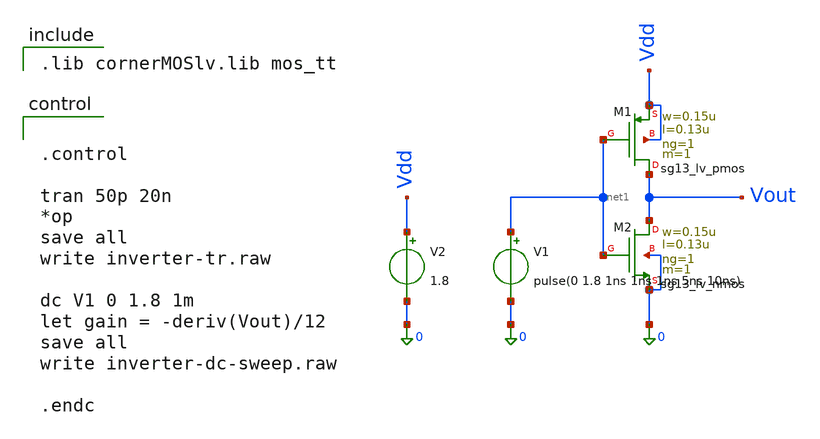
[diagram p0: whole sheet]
** sch_path: designs/inverter/inverter.sch
**.subckt inverter
XM1 Vout net1 Vdd Vdd sg13_lv_pmos w=0.15u l=0.13u ng=1 m=1 mm_ok=1
XM2 Vout net1 0 0 sg13_lv_nmos w=0.15u l=0.13u ng=1 m=1 mm_ok=1
V1 net1 0 pulse(0 1.8 1ns 1ns 1ns 5ns 10ns)
V2 Vdd 0 1.8
**** begin user architecture code

.lib cornerMOSlv.lib mos_tt



.control

tran 50p 20n
*op
save all
write inverter-tr.raw

dc V1 0 1.8 1m
let gain = -deriv(Vout)/12
save all
write inverter-dc-sweep.raw

.endc


**** end user architecture code
**.ends
.end
